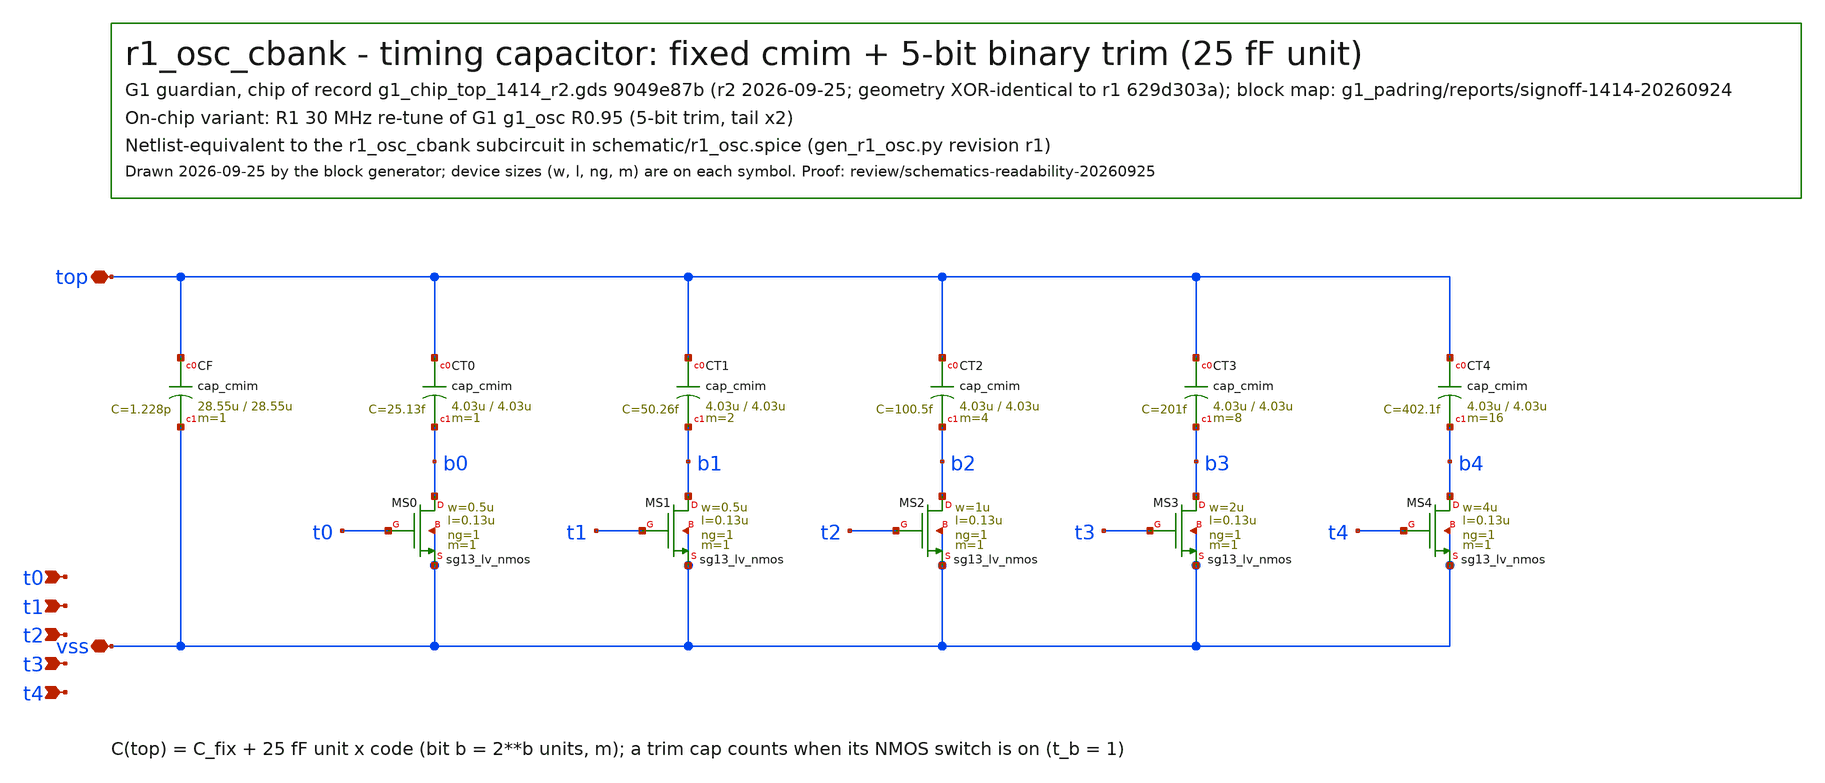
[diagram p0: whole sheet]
** sch_path: designs/r1-joint/blocks/r1_osc/schematic/r1_osc_cbank.sch
**.subckt r1_osc_cbank t0 t1 t2 t3 t4 top vss
*.ipin t0
*.ipin t1
*.ipin t2
*.ipin t3
*.ipin t4
*.iopin top
*.iopin vss
XCF top vss cap_cmim w=28.55u l=28.55u m=1 mm_ok=1
XCT0 top b0 cap_cmim w=4.03u l=4.03u m=1 mm_ok=1
XMS0 b0 t0 vss vss sg13_lv_nmos w=0.5u l=0.13u ng=1 m=1 mm_ok=1
XCT1 top b1 cap_cmim w=4.03u l=4.03u m=2 mm_ok=1
XMS1 b1 t1 vss vss sg13_lv_nmos w=0.5u l=0.13u ng=1 m=1 mm_ok=1
XCT2 top b2 cap_cmim w=4.03u l=4.03u m=4 mm_ok=1
XMS2 b2 t2 vss vss sg13_lv_nmos w=1u l=0.13u ng=1 m=1 mm_ok=1
XCT3 top b3 cap_cmim w=4.03u l=4.03u m=8 mm_ok=1
XMS3 b3 t3 vss vss sg13_lv_nmos w=2u l=0.13u ng=1 m=1 mm_ok=1
XCT4 top b4 cap_cmim w=4.03u l=4.03u m=16 mm_ok=1
XMS4 b4 t4 vss vss sg13_lv_nmos w=4u l=0.13u ng=1 m=1 mm_ok=1
**.ends
.end
